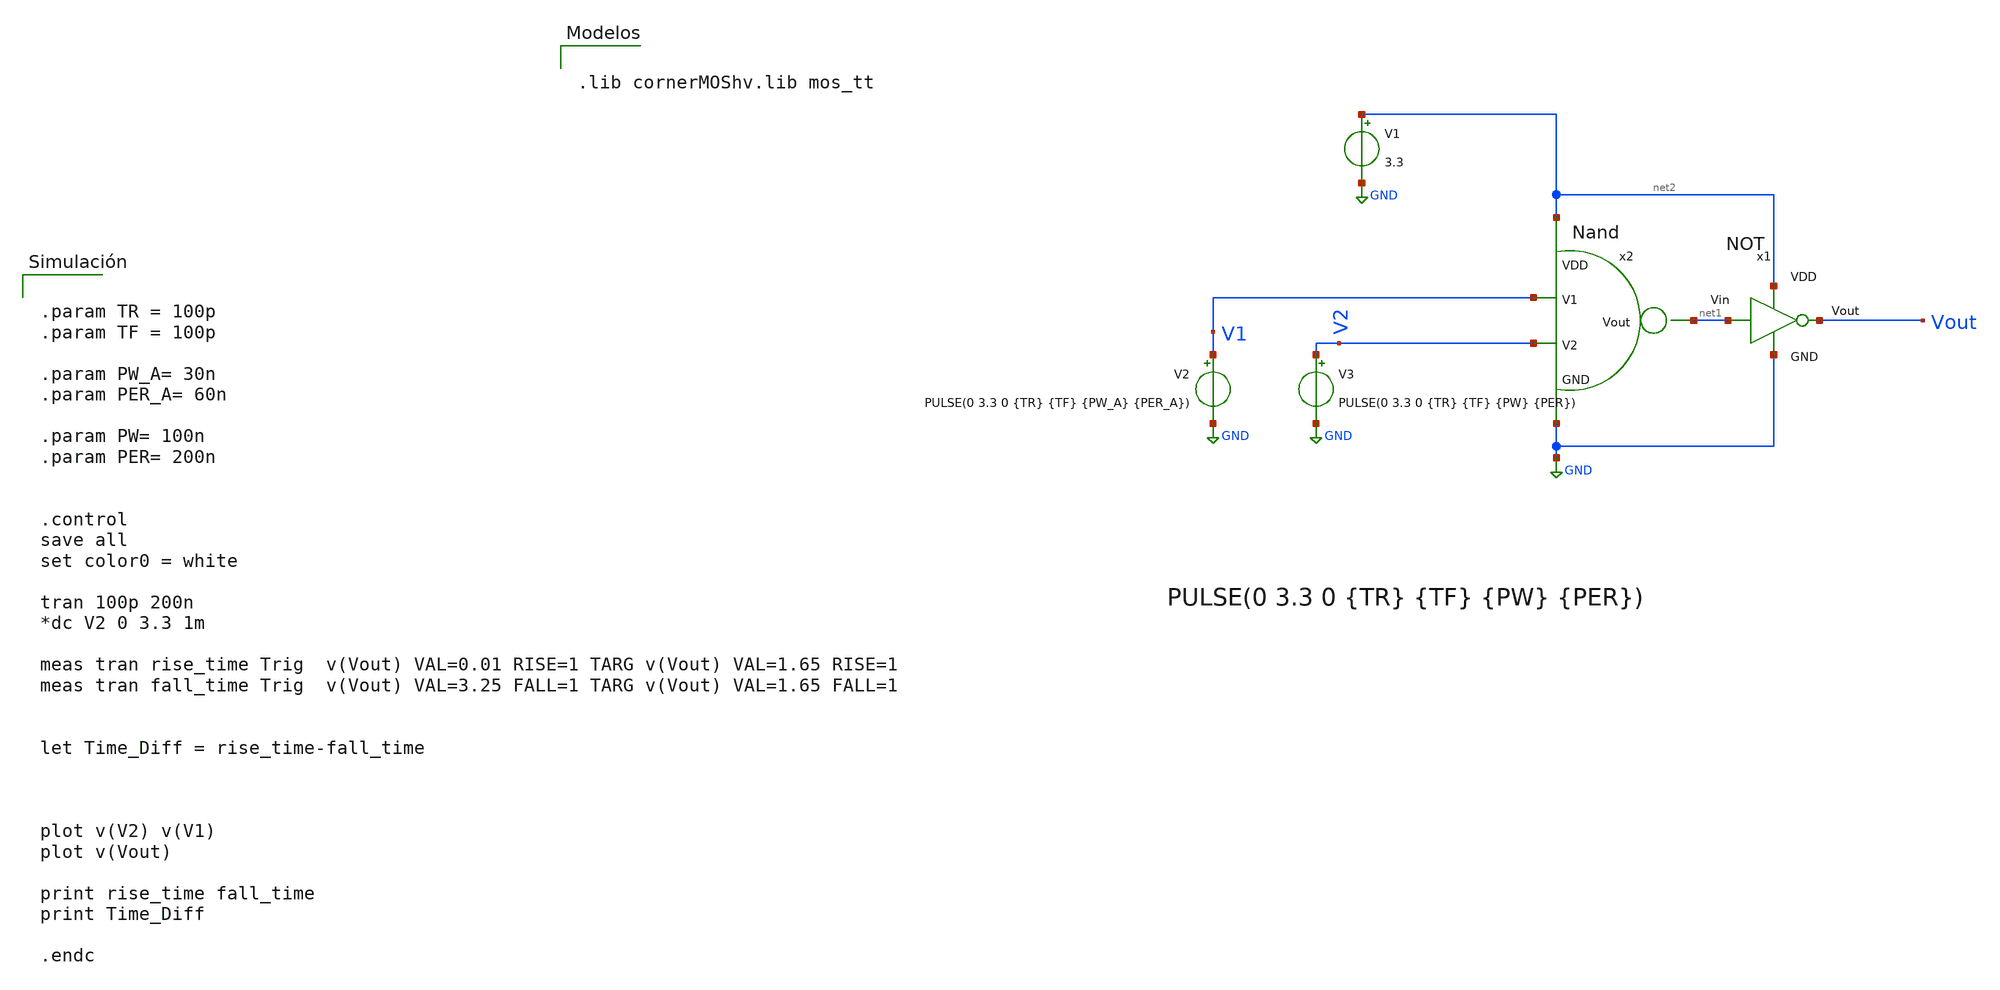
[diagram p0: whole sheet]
** sch_path: Taller2/Resuelto/Testbench_AND.sch
**.subckt Testbench_AND
x1 net2 net1 Vout GND NOT
x2 net2 net1 V1 V2 GND Nand
V1 net2 GND 3.3
V3 V2 GND PULSE(0 3.3 0 {TR} {TF} {PW} {PER})
V2 V1 GND PULSE(0 3.3 0 {TR} {TF} {PW_A} {PER_A})
**** begin user architecture code


.param TR = 100p
.param TF = 100p

.param PW_A= 30n
.param PER_A= 60n

.param PW= 100n
.param PER= 200n


.control
save all
set color0 = white

tran 100p 200n
*dc V2 0 3.3 1m

meas tran rise_time Trig  v(Vout) VAL=0.01 RISE=1 TARG v(Vout) VAL=1.65 RISE=1
meas tran fall_time Trig  v(Vout) VAL=3.25 FALL=1 TARG v(Vout) VAL=1.65 FALL=1


let Time_Diff = rise_time-fall_time



plot v(V2) v(V1)
plot v(Vout)

print rise_time fall_time
print Time_Diff

.endc




.lib cornerMOShv.lib mos_tt


**** end user architecture code
**.ends

* expanding   symbol:  /home/designer/shared/Taller2/NOT.sym # of pins=4
** sym_path: Taller2/Insumos/NOT.sym
** sch_path: Taller2/Insumos/NOT.sch
.subckt NOT VDD Vin Vout GND
*.ipin VDD
*.ipin Vin
*.ipin GND
*.opin Vout
XM3 GND Vin Vout GND sg13_hv_nmos w=1.0u l=0.45u ng=1 m=1 mm_ok=1
XM4 Vout Vin VDD VDD sg13_hv_pmos w=2.72u l=0.45u ng=1 m=1 mm_ok=1
.ends


* expanding   symbol:  /home/designer/shared/Taller2/Nand.sym # of pins=5
** sym_path: Taller2/Resuelto/Nand.sym
** sch_path: Taller2/Resuelto/Nand.sch
.subckt Nand VDD Vout V1 V2 GND
*.ipin V1
*.ipin V2
*.ipin VDD
*.ipin GND
*.opin Vout
XM1 Vout V1 net1 GND sg13_hv_nmos w=1.0u l=0.45u ng=1 m=1 mm_ok=1
XM2 Vout V1 VDD VDD sg13_hv_pmos w=2.72u l=0.45u ng=1 m=1 mm_ok=1
XM3 Vout V2 VDD VDD sg13_hv_pmos w=2.72u l=0.45u ng=1 m=1 mm_ok=1
XM4 net1 V2 GND GND sg13_hv_nmos w=1.0u l=0.45u ng=1 m=1 mm_ok=1
.ends

.GLOBAL GND
.end
